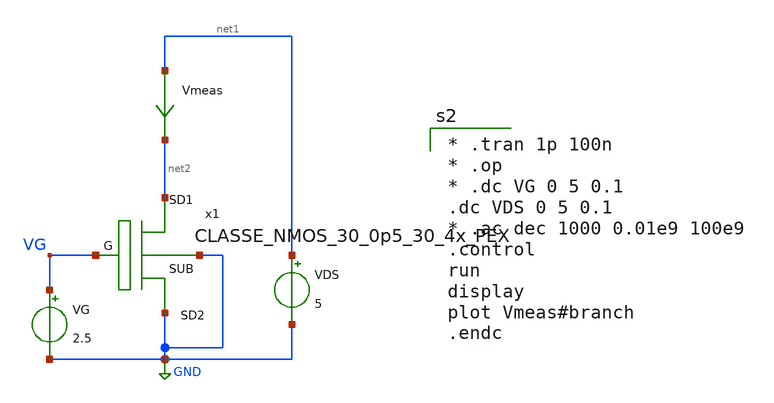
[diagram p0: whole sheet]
** sch_path: xschem/CLASSE_transistor_test.sch
**.subckt CLASSE_transistor_test
x1 net2 GND VG GND CLASSE_NMOS_30_0p5_30_4x_PEX
VDS net1 GND 5
VG VG GND 2.5
Vmeas net1 net2 0
.save i(vmeas)
**** begin user architecture code
.lib $::SKYWATER_MODELS/sky130.lib.spice tt
* .include /home/al/openmpw/pdk_1/sky130B/libs.ref/sky130_fd_sc_hd/spice/sky130_fd_sc_hd.spice


* .tran 1p 100n
* .op
* .dc VG 0 5 0.1
.dc VDS 0 5 0.1
* .ac dec 1000 0.01e9 100e9
.control
run
display
plot Vmeas#branch
.endc


**** end user architecture code
**.ends

* expanding   symbol:  CLASSE_NMOS_30_0p5_30_4x_PEX.sym # of pins=4
** sym_path: ClassE_DataExchange/220920_NMOS_30_0p5_30_4x_models/Xschem Simulation Model/CLASSE_NMOS_30_0p5_30_4x_PEX.sym
** sch_path: ClassE_DataExchange/220920_NMOS_30_0p5_30_4x_models/Xschem Simulation Model/CLASSE_NMOS_30_0p5_30_4x_PEX.sch
.subckt CLASSE_NMOS_30_0p5_30_4x_PEX SD1 SD2 G SUB
*.iopin SD1
*.iopin SD2
*.iopin G
*.iopin SUB
**** begin user architecture code

.subckt NMOS_30_0p5_30_4x SD2 G SD1 SUB
    .subckt NMOS_30_0p5_30_1 SD2 G SD1 SUB
        X0 SD2 G SD1 SUB sky130_fd_pr__nfet_g5v0d10v5 ad=0p pd=0u as=0p ps=0u w=3e+07u l=500000u
        X1 SD2 G SD1 SUB sky130_fd_pr__nfet_g5v0d10v5 ad=0p pd=0u as=0p ps=0u w=3e+07u l=500000u
        X2 SD1 G SD2 SUB sky130_fd_pr__nfet_g5v0d10v5 ad=0p pd=0u as=0p ps=0u w=3e+07u l=500000u
        X3 SD1 G SD2 SUB sky130_fd_pr__nfet_g5v0d10v5 ad=0p pd=0u as=0p ps=0u w=3e+07u l=500000u
        X4 SD2 G SD1 SUB sky130_fd_pr__nfet_g5v0d10v5 ad=0p pd=0u as=0p ps=0u w=3e+07u l=500000u
        X5 SD2 G SD1 SUB sky130_fd_pr__nfet_g5v0d10v5 ad=0p pd=0u as=0p ps=0u w=3e+07u l=500000u
        X6 SD2 G SD1 SUB sky130_fd_pr__nfet_g5v0d10v5 ad=0p pd=0u as=0p ps=0u w=3e+07u l=500000u
        X7 SD2 G SD1 SUB sky130_fd_pr__nfet_g5v0d10v5 ad=0p pd=0u as=0p ps=0u w=3e+07u l=500000u
        X8 SD1 G SD2 SUB sky130_fd_pr__nfet_g5v0d10v5 ad=0p pd=0u as=0p ps=0u w=3e+07u l=500000u
        X9 SD1 G SD2 SUB sky130_fd_pr__nfet_g5v0d10v5 ad=0p pd=0u as=0p ps=0u w=3e+07u l=500000u
        X10 SD2 G SD1 SUB sky130_fd_pr__nfet_g5v0d10v5 ad=0p pd=0u as=0p ps=0u w=3e+07u l=500000u
        X11 SD1 G SD2 SUB sky130_fd_pr__nfet_g5v0d10v5 ad=0p pd=0u as=0p ps=0u w=3e+07u l=500000u
        X12 SD1 G SD2 SUB sky130_fd_pr__nfet_g5v0d10v5 ad=0p pd=0u as=0p ps=0u w=3e+07u l=500000u
        X13 SD2 G SD1 SUB sky130_fd_pr__nfet_g5v0d10v5 ad=0p pd=0u as=0p ps=0u w=3e+07u l=500000u
        X14 SD2 G SD1 SUB sky130_fd_pr__nfet_g5v0d10v5 ad=0p pd=0u as=0p ps=0u w=3e+07u l=500000u
        X15 SD2 G SD1 SUB sky130_fd_pr__nfet_g5v0d10v5 ad=0p pd=0u as=0p ps=0u w=3e+07u l=500000u
        X16 SD1 G SD2 SUB sky130_fd_pr__nfet_g5v0d10v5 ad=0p pd=0u as=0p ps=0u w=3e+07u l=500000u
        X17 SD1 G SD2 SUB sky130_fd_pr__nfet_g5v0d10v5 ad=0p pd=0u as=0p ps=0u w=3e+07u l=500000u
        X18 SD2 G SD1 SUB sky130_fd_pr__nfet_g5v0d10v5 ad=0p pd=0u as=0p ps=0u w=3e+07u l=500000u
        X19 SD1 G SD2 SUB sky130_fd_pr__nfet_g5v0d10v5 ad=0p pd=0u as=0p ps=0u w=3e+07u l=500000u
        X20 SD1 G SD2 SUB sky130_fd_pr__nfet_g5v0d10v5 ad=0p pd=0u as=0p ps=0u w=3e+07u l=500000u
        X21 SD2 G SD1 SUB sky130_fd_pr__nfet_g5v0d10v5 ad=0p pd=0u as=0p ps=0u w=3e+07u l=500000u
        X22 SD1 G SD2 SUB sky130_fd_pr__nfet_g5v0d10v5 ad=0p pd=0u as=0p ps=0u w=3e+07u l=500000u
        X23 SD1 G SD2 SUB sky130_fd_pr__nfet_g5v0d10v5 ad=0p pd=0u as=0p ps=0u w=3e+07u l=500000u
        X24 SD1 G SD2 SUB sky130_fd_pr__nfet_g5v0d10v5 ad=0p pd=0u as=0p ps=0u w=3e+07u l=500000u
        X25 SD1 G SD2 SUB sky130_fd_pr__nfet_g5v0d10v5 ad=0p pd=0u as=0p ps=0u w=3e+07u l=500000u
        X26 SD1 G SD2 SUB sky130_fd_pr__nfet_g5v0d10v5 ad=0p pd=0u as=0p ps=0u w=3e+07u l=500000u
        X27 SD2 G SD1 SUB sky130_fd_pr__nfet_g5v0d10v5 ad=0p pd=0u as=0p ps=0u w=3e+07u l=500000u
        X28 SD2 G SD1 SUB sky130_fd_pr__nfet_g5v0d10v5 ad=0p pd=0u as=0p ps=0u w=3e+07u l=500000u
        X29 SD2 G SD1 SUB sky130_fd_pr__nfet_g5v0d10v5 ad=0p pd=0u as=0p ps=0u w=3e+07u l=500000u
        C0 SD1 SD2 195.54fF
        C1 G SD1 19.19fF
        C2 G SD2 18.07fF
        C3 SD1 SUB 1.73fF $ **FLOATING
        C4 SD2 SUB 16.40fF $ **FLOATING
        C5 G SUB 23.59fF $ **FLOATING
    .ends
    XDUT_sub_0 SD2 G SD1 SUB NMOS_30_0p5_30_1
    XDUT_sub_1 SD2 G SD1 SUB NMOS_30_0p5_30_1
    XDUT_sub_2 SD2 G SD1 SUB NMOS_30_0p5_30_1
    XDUT_sub_3 SD2 G SD1 SUB NMOS_30_0p5_30_1
.ends

XDUT SD2 G SD1 SUB NMOS_30_0p5_30_4x




**** end user architecture code
.ends

.GLOBAL GND
.end
